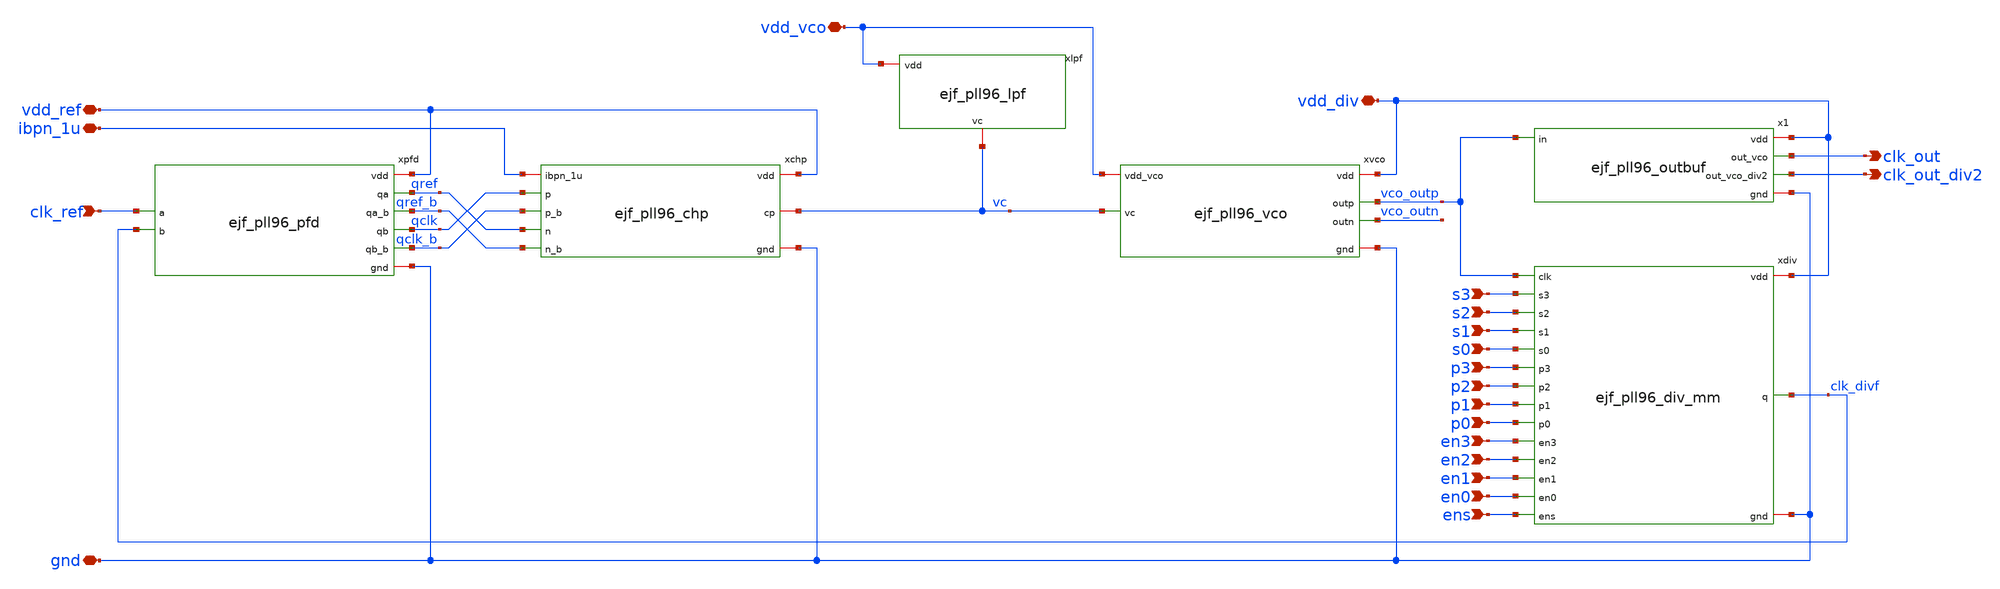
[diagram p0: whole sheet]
** sch_path: xschem/ejf_pll96.sch
**.subckt ejf_pll96 vdd_ref vdd_vco vdd_div gnd ibpn_1u clk_ref s3 s2 s1 s0 p3 p2 p1 p0 en3 en2 en1
*+ en0 ens clk_out clk_out_div2
*.iopin vdd_ref
*.iopin vdd_vco
*.iopin vdd_div
*.iopin gnd
*.iopin ibpn_1u
*.ipin clk_ref
*.ipin s3
*.ipin s2
*.ipin s1
*.ipin s0
*.ipin p3
*.ipin p2
*.ipin p1
*.ipin p0
*.ipin en3
*.ipin en2
*.ipin en1
*.ipin en0
*.ipin ens
*.opin clk_out
*.opin clk_out_div2
xlpf vdd_vco vc ejf_pll96_lpf
xdiv p3 vco_outp p2 p1 clk_divf p0 en3 en2 en1 s3 s2 s1 s0 vdd_div gnd en0 ens ejf_pll96_div_mm
xpfd qref clk_ref qclk clk_divf vdd_ref gnd qref_b qclk_b ejf_pll96_pfd
xchp vdd_ref qclk_b qclk vc ibpn_1u qref_b qref gnd ejf_pll96_chp
xvco vdd_vco vc vdd_div vco_outp vco_outn gnd ejf_pll96_vco
x1 vco_outp clk_out clk_out_div2 vdd_div gnd ejf_pll96_outbuf
**.ends
.end
